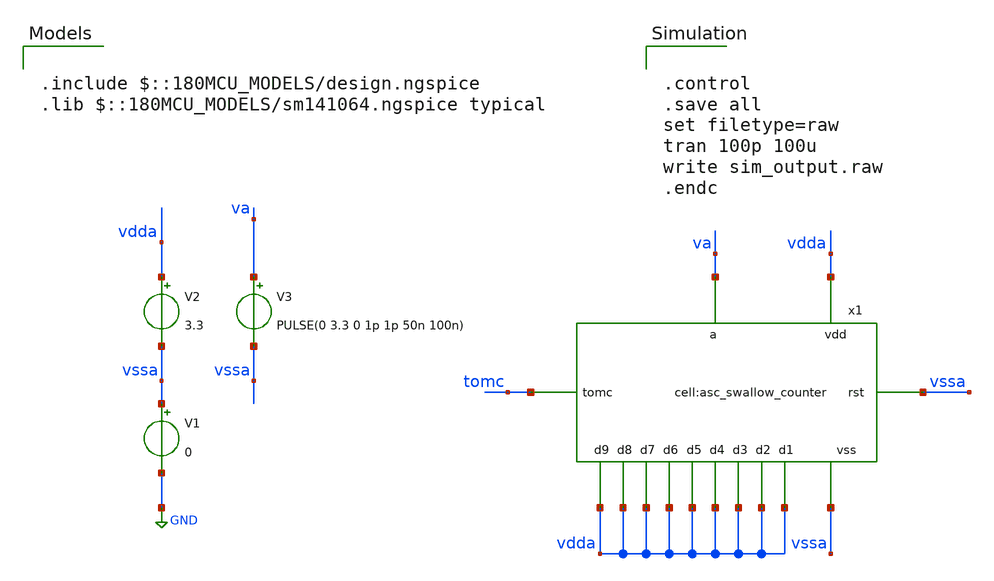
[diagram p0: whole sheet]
** sch_path: designs/libs/tb_analog/tb_asc_swallow_counter/tb_asc_swallow_counter.sch
**.subckt tb_asc_swallow_counter
V1 vssa GND 0
V2 vdda vssa 3.3
V3 va vssa PULSE(0 3.3 0 1p 1p 50n 100n)
x1 tomc vdda vdda vdda vdda vdda vdda vdda vdda vdda vssa vssa vdda va asc_swallow_counter
**** begin user architecture code

.include $::180MCU_MODELS/design.ngspice
.lib $::180MCU_MODELS/sm141064.ngspice typical



.control
.save all
set filetype=raw
tran 100p 100u
write sim_output.raw
.endc


**** end user architecture code
**.ends
.GLOBAL GND
.end
